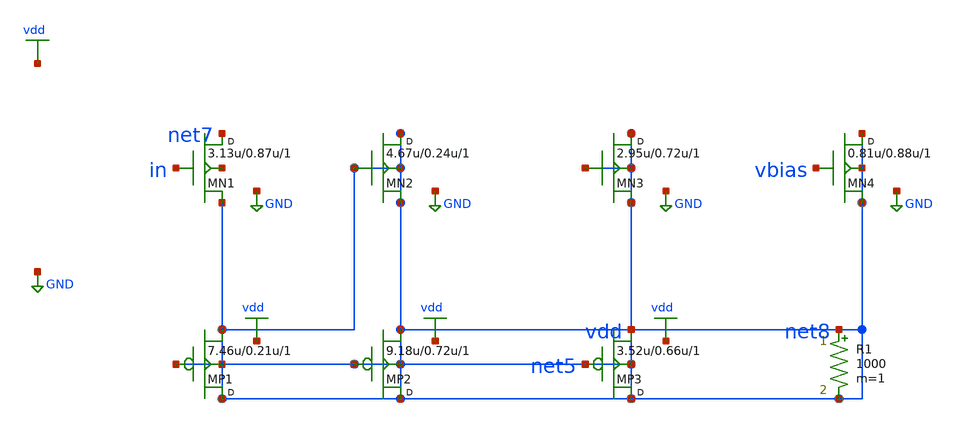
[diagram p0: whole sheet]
** sch_path: synthetic/generated/0041_synthetic.sch
**.subckt 0041_synthetic
MN1 net7 in net5 net1 nmos w=3.13u l=0.87u m=1
MN2 net5 net5 net5 net5 nmos w=4.67u l=0.24u m=1
MN3 net5 net5 net5 net5 nmos w=2.95u l=0.72u m=1
MN4 net5 vbias net5 net5 nmos w=0.81u l=0.88u m=1
MP1 net5 net5 net5 net5 pmos w=7.46u l=0.21u m=1
MP2 net5 net5 net5 net5 pmos w=9.18u l=0.72u m=1
MP3 net5 net5 net5 net5 pmos w=3.52u l=0.66u m=1
R1 net5 net5 1000 m=1
**.ends
.GLOBAL GND
.GLOBAL vdd
.end
